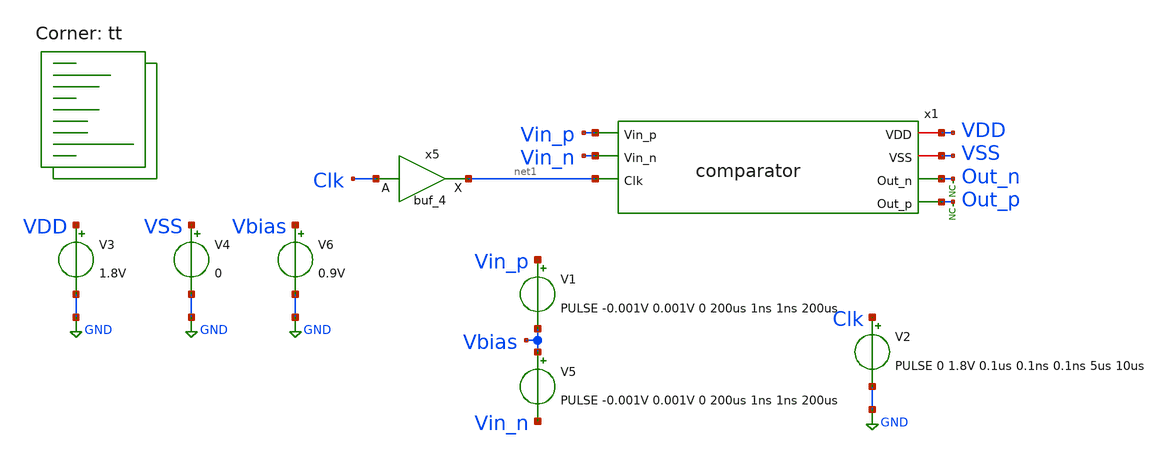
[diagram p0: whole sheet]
** sch_path: xschem/tests/comparator/comparator_test_small_v.sch
**.subckt comparator_test_small_v
V3 VDD GND 1.8V
V4 VSS GND 0
x1 VDD VSS Vin_p Out_n Vin_n Out_p net1 comparator
V1 Vin_p Vbias PULSE -0.001V 0.001V 0 200us 1ns 1ns 200us
V2 Clk GND PULSE 0 1.8V 0.1us 0.1ns 0.1ns 5us 10us
* noconn Out_p
* noconn Out_n
V5 Vbias Vin_n PULSE -0.001V 0.001V 0 200us 1ns 1ns 200us
V6 Vbias GND 0.9V
x5 Clk VSS VSS VDD VDD net1 sky130_fd_sc_hd__buf_4
**** begin user architecture code
 *.lib $::SKYWATER_MODELS/sky130.lib.spice tt
.include $::SKYWATER_STDCELLS/sky130_fd_sc_hd.spice


.options acct list
.options method=gear
.temp 25
*vvcc VDD 0 dc 1.8
*vvss VSS 0 0
.control
save all
tran 0.1u 200u
*dc V1 0 1.8V 0.1
plot Vin_p-Vin_n Out_p-Out_n Clk-4
* plot Vbias Vin_p Vin_n
plot x1.pre_amp_p x1.pre_amp_n+2 clk-2
*plot i(v.x1.v1) i(v.x1.v2)+2 clk-2
plot Vin_p-Vin_n x1.pre_amp_p-x1.pre_amp_n Out_p-Out_n+4 Clk-4
plot Vin_p-Vin_n x1.pre_amp_p-x1.pre_amp_n
plot Vin_p-Vin_n x1.pre_amp_p-x1.pre_amp_n out_p-out_n
write comparator_test_small_v.raw
.endc


.lib $::SKYWATER_MODELS/sky130.lib.spice tt
**** end user architecture code
**.ends

* expanding   symbol:  src/comparator/comparator.sym # of pins=7
** sym_path: xschem/src/comparator/comparator.sym
** sch_path: xschem/src/comparator/comparator.sch
.subckt comparator VDD VSS Vin_p Out_n Vin_n Out_p Clk
*.iopin VDD
*.iopin VSS
*.ipin Vin_p
*.opin Out_n
*.ipin Vin_n
*.opin Out_p
*.ipin Clk
XM1 Pre_Amp_n Clk VDD VSS sky130_fd_pr__pfet_01v8 L=0.15 W=1 nf=1 ad='int((nf+1)/2) * W/nf * 0.29' as='int((nf+2)/2) * W/nf * 0.29'
+ pd='2*int((nf+1)/2) * (W/nf + 0.29)' ps='2*int((nf+2)/2) * (W/nf + 0.29)' nrd='0.29 / W' nrs='0.29 / W'
+ sa=0 sb=0 sd=0 mult=1 m=1
XM2 Pre_Amp_p Clk VDD VSS sky130_fd_pr__pfet_01v8 L=0.15 W=1 nf=1 ad='int((nf+1)/2) * W/nf * 0.29' as='int((nf+2)/2) * W/nf * 0.29'
+ pd='2*int((nf+1)/2) * (W/nf + 0.29)' ps='2*int((nf+2)/2) * (W/nf + 0.29)' nrd='0.29 / W' nrs='0.29 / W'
+ sa=0 sb=0 sd=0 mult=1 m=1
XM3 Pre_Amp_p Vin_p net1 VSS sky130_fd_pr__nfet_01v8 L=0.15 W=1 nf=1 ad='int((nf+1)/2) * W/nf * 0.29'
+ as='int((nf+2)/2) * W/nf * 0.29' pd='2*int((nf+1)/2) * (W/nf + 0.29)' ps='2*int((nf+2)/2) * (W/nf + 0.29)'
+ nrd='0.29 / W' nrs='0.29 / W' sa=0 sb=0 sd=0 mult=1 m=1
XM4 Pre_Amp_n Vin_n net1 VSS sky130_fd_pr__nfet_01v8 L=0.15 W=1 nf=1 ad='int((nf+1)/2) * W/nf * 0.29'
+ as='int((nf+2)/2) * W/nf * 0.29' pd='2*int((nf+1)/2) * (W/nf + 0.29)' ps='2*int((nf+2)/2) * (W/nf + 0.29)'
+ nrd='0.29 / W' nrs='0.29 / W' sa=0 sb=0 sd=0 mult=1 m=1
XM5 net3 Out_p VDD VSS sky130_fd_pr__pfet_01v8 L=0.15 W=1 nf=1 ad='int((nf+1)/2) * W/nf * 0.29' as='int((nf+2)/2) * W/nf * 0.29'
+ pd='2*int((nf+1)/2) * (W/nf + 0.29)' ps='2*int((nf+2)/2) * (W/nf + 0.29)' nrd='0.29 / W' nrs='0.29 / W'
+ sa=0 sb=0 sd=0 mult=1 m=1
XM6 net2 Out_n VDD VSS sky130_fd_pr__pfet_01v8 L=0.15 W=1 nf=1 ad='int((nf+1)/2) * W/nf * 0.29' as='int((nf+2)/2) * W/nf * 0.29'
+ pd='2*int((nf+1)/2) * (W/nf + 0.29)' ps='2*int((nf+2)/2) * (W/nf + 0.29)' nrd='0.29 / W' nrs='0.29 / W'
+ sa=0 sb=0 sd=0 mult=1 m=1
XM7 net2 Pre_Amp_p Out_p VSS sky130_fd_pr__nfet_01v8 L=0.15 W=1 nf=1 ad='int((nf+1)/2) * W/nf * 0.29'
+ as='int((nf+2)/2) * W/nf * 0.29' pd='2*int((nf+1)/2) * (W/nf + 0.29)' ps='2*int((nf+2)/2) * (W/nf + 0.29)'
+ nrd='0.29 / W' nrs='0.29 / W' sa=0 sb=0 sd=0 mult=1 m=1
XM8 net3 Pre_Amp_n Out_n VSS sky130_fd_pr__nfet_01v8 L=0.15 W=1 nf=1 ad='int((nf+1)/2) * W/nf * 0.29'
+ as='int((nf+2)/2) * W/nf * 0.29' pd='2*int((nf+1)/2) * (W/nf + 0.29)' ps='2*int((nf+2)/2) * (W/nf + 0.29)'
+ nrd='0.29 / W' nrs='0.29 / W' sa=0 sb=0 sd=0 mult=1 m=1
XM9 net1 Clk VSS VSS sky130_fd_pr__nfet_01v8 L=0.15 W=1 nf=1 ad='int((nf+1)/2) * W/nf * 0.29' as='int((nf+2)/2) * W/nf * 0.29'
+ pd='2*int((nf+1)/2) * (W/nf + 0.29)' ps='2*int((nf+2)/2) * (W/nf + 0.29)' nrd='0.29 / W' nrs='0.29 / W'
+ sa=0 sb=0 sd=0 mult=1 m=1
XM10 Pre_Amp_n Vin_n net1 VSS sky130_fd_pr__nfet_01v8 L=0.15 W=1 nf=1 ad='int((nf+1)/2) * W/nf * 0.29'
+ as='int((nf+2)/2) * W/nf * 0.29' pd='2*int((nf+1)/2) * (W/nf + 0.29)' ps='2*int((nf+2)/2) * (W/nf + 0.29)'
+ nrd='0.29 / W' nrs='0.29 / W' sa=0 sb=0 sd=0 mult=1 m=1
XM11 Out_n Clk_n VSS VSS sky130_fd_pr__nfet_01v8 L=0.15 W=1 nf=1 ad='int((nf+1)/2) * W/nf * 0.29' as='int((nf+2)/2) * W/nf * 0.29'
+ pd='2*int((nf+1)/2) * (W/nf + 0.29)' ps='2*int((nf+2)/2) * (W/nf + 0.29)' nrd='0.29 / W' nrs='0.29 / W'
+ sa=0 sb=0 sd=0 mult=1 m=1
XM12 Out_n Out_p VSS VSS sky130_fd_pr__nfet_01v8 L=0.15 W=1 nf=1 ad='int((nf+1)/2) * W/nf * 0.29' as='int((nf+2)/2) * W/nf * 0.29'
+ pd='2*int((nf+1)/2) * (W/nf + 0.29)' ps='2*int((nf+2)/2) * (W/nf + 0.29)' nrd='0.29 / W' nrs='0.29 / W'
+ sa=0 sb=0 sd=0 mult=1 m=1
XM13 Out_p Out_n VSS VSS sky130_fd_pr__nfet_01v8 L=0.15 W=1 nf=1 ad='int((nf+1)/2) * W/nf * 0.29' as='int((nf+2)/2) * W/nf * 0.29'
+ pd='2*int((nf+1)/2) * (W/nf + 0.29)' ps='2*int((nf+2)/2) * (W/nf + 0.29)' nrd='0.29 / W' nrs='0.29 / W'
+ sa=0 sb=0 sd=0 mult=1 m=1
XM14 Out_p Clk_n VSS VSS sky130_fd_pr__nfet_01v8 L=0.15 W=1 nf=1 ad='int((nf+1)/2) * W/nf * 0.29' as='int((nf+2)/2) * W/nf * 0.29'
+ pd='2*int((nf+1)/2) * (W/nf + 0.29)' ps='2*int((nf+2)/2) * (W/nf + 0.29)' nrd='0.29 / W' nrs='0.29 / W'
+ sa=0 sb=0 sd=0 mult=1 m=1
XM15 Clk_n Clk VDD VSS sky130_fd_pr__pfet_01v8 L=0.15 W=1 nf=1 ad='int((nf+1)/2) * W/nf * 0.29' as='int((nf+2)/2) * W/nf * 0.29'
+ pd='2*int((nf+1)/2) * (W/nf + 0.29)' ps='2*int((nf+2)/2) * (W/nf + 0.29)' nrd='0.29 / W' nrs='0.29 / W'
+ sa=0 sb=0 sd=0 mult=1 m=1
XM16 Clk_n Clk VSS VSS sky130_fd_pr__nfet_01v8 L=0.15 W=1 nf=1 ad='int((nf+1)/2) * W/nf * 0.29' as='int((nf+2)/2) * W/nf * 0.29'
+ pd='2*int((nf+1)/2) * (W/nf + 0.29)' ps='2*int((nf+2)/2) * (W/nf + 0.29)' nrd='0.29 / W' nrs='0.29 / W'
+ sa=0 sb=0 sd=0 mult=1 m=1
.ends

.GLOBAL GND
.end
